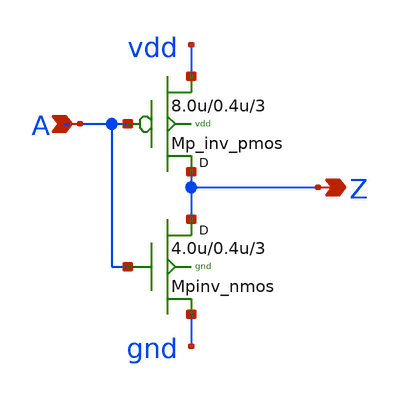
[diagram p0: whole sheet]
** sch_path: sram_2_16_scn4m/pinv_7.sch
**.subckt pinv_7 A Z
*.ipin A
*.opin Z
Mpinv_nmos Z A gnd gnd n w=4.0u l=0.4u m=3
Mp_inv_pmos Z A vdd vdd p w=8.0u l=0.4u m=3
**.ends
.end
